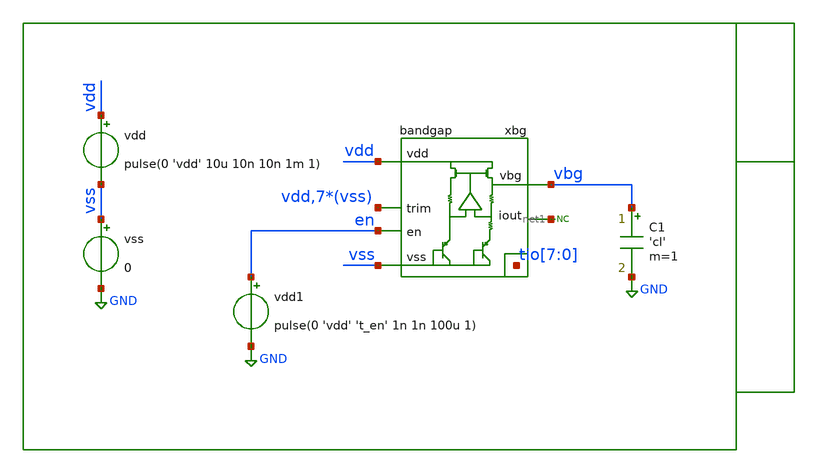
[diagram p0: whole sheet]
** sch_path: xschem/tb/bandgap_cm/bandgap/tr_bandgap_power_off.sch
**.subckt tr_bandgap_power_off
xbg vdd vbg vss tio[7] tio[6] tio[5] tio[4] tio[3] tio[2] tio[1] tio[0] vdd vss vss vss vss vss vss
+ vss net1 en bandgap
vss vss GND 0
C1 vbg GND 'cl' m=1
vdd vdd vss pulse(0 'vdd' 10u 10n 10n 1m 1)
* noconn #net1
vdd1 en GND pulse(0 'vdd' 't_en' 1n 1n 100u 1)
**** begin user architecture code

* Control

.param vdd = 3.3
.param cl = 500e-15

.param t_en = 20u
.csparam t_en = t_en

.temp 27
.options reltol = 1e-6
.options abstol = 1e-12
.options gmin = 1e-15
.options method = gear

.control
save all
tran 1u 1m

let ivdd = abs(vdd#branch)
meas tran ivdd_ss find ivdd at=999e-6

print ivdd_ss

set wr_singlescale
set wr_vecnames
wrdata data.csv vbg ivdd

.endc
.end


 * Model Corners

.include $::CORNERS/ngspice/tt.spice
*.include $::CORNERS/ngspice/ff.spice
*.include $::CORNERS/ngspice/ss.spice
*.include $::CORNERS/ngspice/sf.spice
*.include $::CORNERS/ngspice/fs.spice

**** end user architecture code
**.ends
.GLOBAL GND
.end
